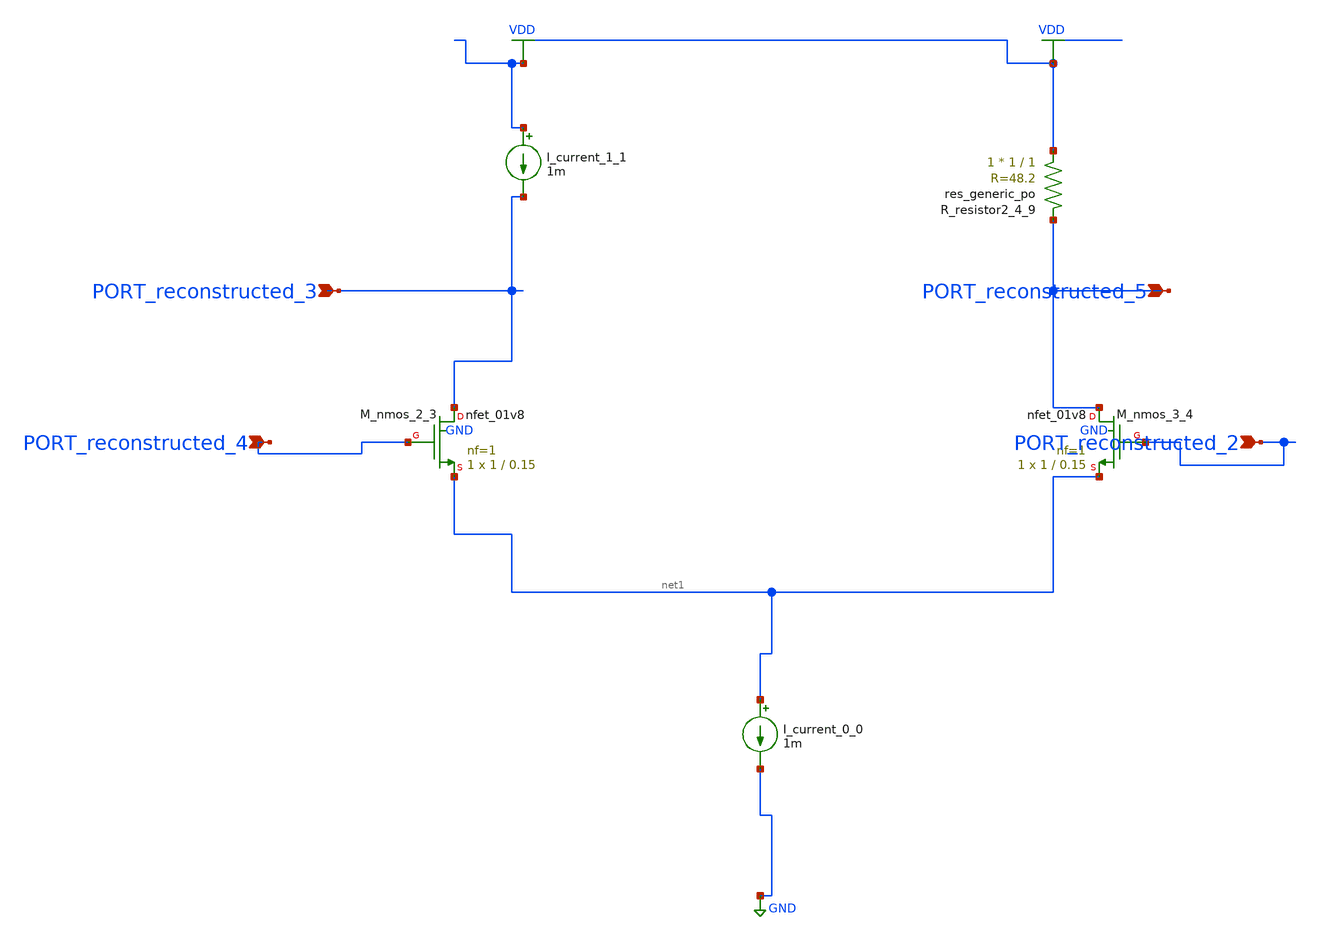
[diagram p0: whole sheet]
** sch_path: schematics/AMSNet/251.sch
**.subckt 251 PORT_reconstructed_2 PORT_reconstructed_3 PORT_reconstructed_4 PORT_reconstructed_5
*.ipin PORT_reconstructed_2
*.ipin PORT_reconstructed_3
*.ipin PORT_reconstructed_4
*.ipin PORT_reconstructed_5
I_current_0_0 net1 GND 1m
I_current_1_1 VDD PORT_reconstructed_3 1m
XM_nmos_2_3 PORT_reconstructed_3 PORT_reconstructed_4 net1 GND sky130_fd_pr__nfet_01v8 L=0.15 W=1 nf=1
+ ad='int((1 + 1)/2) * 1 / 1 * 0.29' as='int((1 + 2)/2) * 1 / 1 * 0.29' pd='2*int((1 + 1)/2) * (1 / 1 + 0.29)'
+ ps='2*int((1 + 2)/2) * (1 / 1 + 0.29)' nrd='0.29 / 1 ' nrs='0.29 / 1 ' sa=0 sb=0 sd=0 mult=1 m=1
XM_nmos_3_4 PORT_reconstructed_5 PORT_reconstructed_2 net1 GND sky130_fd_pr__nfet_01v8 L=0.15 W=1 nf=1
+ ad='int((1 + 1)/2) * 1 / 1 * 0.29' as='int((1 + 2)/2) * 1 / 1 * 0.29' pd='2*int((1 + 1)/2) * (1 / 1 + 0.29)'
+ ps='2*int((1 + 2)/2) * (1 / 1 + 0.29)' nrd='0.29 / 1 ' nrs='0.29 / 1 ' sa=0 sb=0 sd=0 mult=1 m=1
XR_resistor2_4_9 VDD PORT_reconstructed_5 sky130_fd_pr__res_generic_po W=1 L=1 m=1
**.ends
.GLOBAL GND
.GLOBAL VDD
.end
